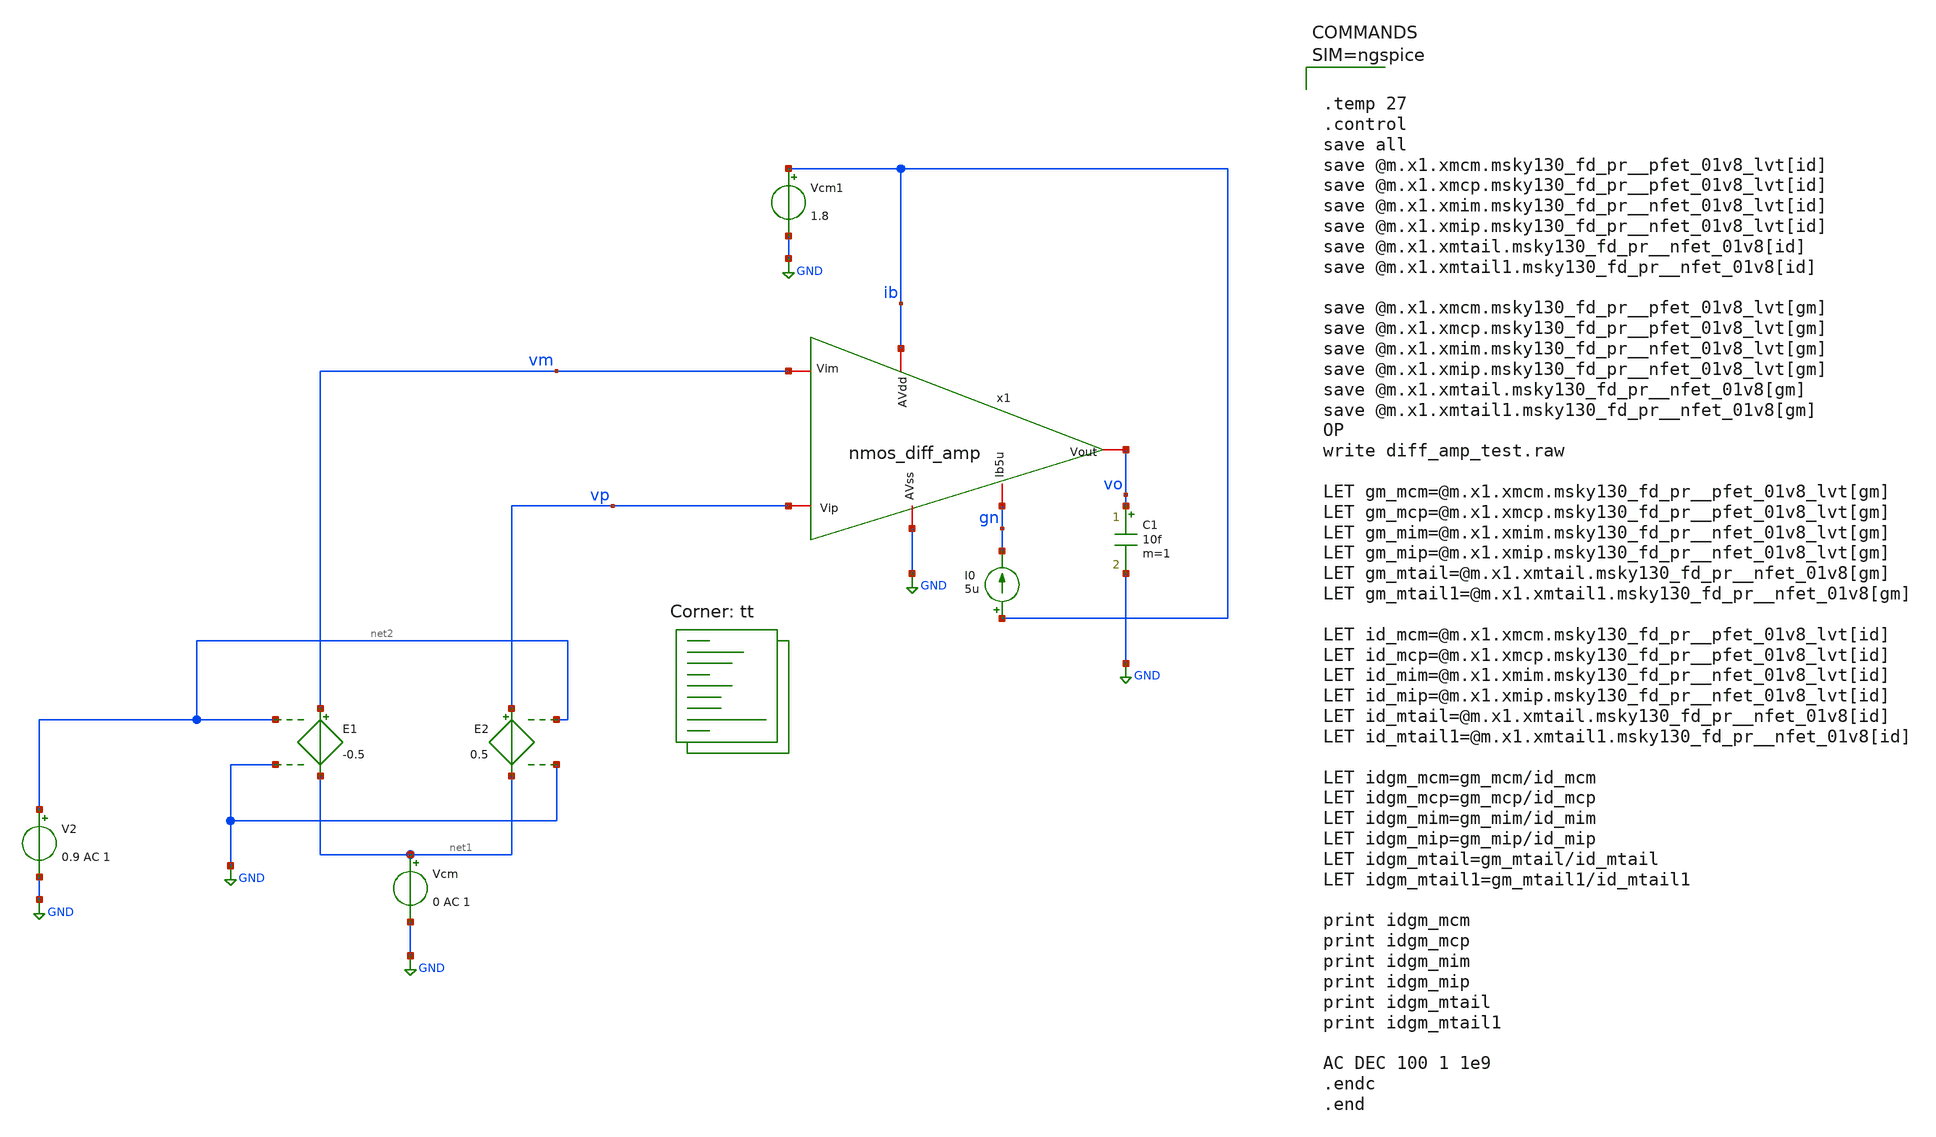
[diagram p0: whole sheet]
** sch_path: Work/xschem/diff_amp_test.sch
**.subckt diff_amp_test
x1 ib vo vm vp gn GND nmos_diff_amp
E1 vm net1 net2 GND -0.5
E2 vp net1 net2 GND 0.5
Vcm net1 GND 0 AC 1
V2 net2 GND 0.9 AC 1
Vcm1 ib GND 1.8
I0 ib gn 5u
C1 vo GND 10f m=1
**** begin user architecture code



.temp 27
.control
save all
save @m.x1.xmcm.msky130_fd_pr__pfet_01v8_lvt[id]
save @m.x1.xmcp.msky130_fd_pr__pfet_01v8_lvt[id]
save @m.x1.xmim.msky130_fd_pr__nfet_01v8_lvt[id]
save @m.x1.xmip.msky130_fd_pr__nfet_01v8_lvt[id]
save @m.x1.xmtail.msky130_fd_pr__nfet_01v8[id]
save @m.x1.xmtail1.msky130_fd_pr__nfet_01v8[id]

save @m.x1.xmcm.msky130_fd_pr__pfet_01v8_lvt[gm]
save @m.x1.xmcp.msky130_fd_pr__pfet_01v8_lvt[gm]
save @m.x1.xmim.msky130_fd_pr__nfet_01v8_lvt[gm]
save @m.x1.xmip.msky130_fd_pr__nfet_01v8_lvt[gm]
save @m.x1.xmtail.msky130_fd_pr__nfet_01v8[gm]
save @m.x1.xmtail1.msky130_fd_pr__nfet_01v8[gm]
OP
write diff_amp_test.raw

LET gm_mcm=@m.x1.xmcm.msky130_fd_pr__pfet_01v8_lvt[gm]
LET gm_mcp=@m.x1.xmcp.msky130_fd_pr__pfet_01v8_lvt[gm]
LET gm_mim=@m.x1.xmim.msky130_fd_pr__nfet_01v8_lvt[gm]
LET gm_mip=@m.x1.xmip.msky130_fd_pr__nfet_01v8_lvt[gm]
LET gm_mtail=@m.x1.xmtail.msky130_fd_pr__nfet_01v8[gm]
LET gm_mtail1=@m.x1.xmtail1.msky130_fd_pr__nfet_01v8[gm]

LET id_mcm=@m.x1.xmcm.msky130_fd_pr__pfet_01v8_lvt[id]
LET id_mcp=@m.x1.xmcp.msky130_fd_pr__pfet_01v8_lvt[id]
LET id_mim=@m.x1.xmim.msky130_fd_pr__nfet_01v8_lvt[id]
LET id_mip=@m.x1.xmip.msky130_fd_pr__nfet_01v8_lvt[id]
LET id_mtail=@m.x1.xmtail.msky130_fd_pr__nfet_01v8[id]
LET id_mtail1=@m.x1.xmtail1.msky130_fd_pr__nfet_01v8[id]

LET idgm_mcm=gm_mcm/id_mcm
LET idgm_mcp=gm_mcp/id_mcp
LET idgm_mim=gm_mim/id_mim
LET idgm_mip=gm_mip/id_mip
LET idgm_mtail=gm_mtail/id_mtail
LET idgm_mtail1=gm_mtail1/id_mtail1

print idgm_mcm
print idgm_mcp
print idgm_mim
print idgm_mip
print idgm_mtail
print idgm_mtail1

AC DEC 100 1 1e9
.endc
.end




.lib $::SKYWATER_MODELS/sky130.lib.spice tt
.lib /usr/local/share/pdk/sky130A/libs.tech/ngspice/sky130.lib.spice tt
**** end user architecture code
**.ends

* expanding   symbol:  nmos_diff_amp.sym # of pins=6
** sym_path: Work/xschem/nmos_diff_amp.sym
** sch_path: Work/xschem/nmos_diff_amp.sch
.subckt nmos_diff_amp AVdd Vout Vim Vip Ib5u AVss
*.iopin AVdd
*.iopin AVss
*.iopin Vim
*.iopin Vip
*.iopin Vout
*.iopin Ib5u
XMip vp Vip io io sky130_fd_pr__nfet_01v8_lvt L=2 W=5 nf=1 ad='int((1 + 1)/2) * 5 / 1 * 0.29' as='int((1 + 2)/2) * 5 / 1 * 0.29'
+ pd='2*int((1 + 1)/2) * (5 / 1 + 0.29)' ps='2*int((1 + 2)/2) * (5 / 1 + 0.29)' nrd='0.29 / 5 ' nrs='0.29 / 5 '
+ sa=0 sb=0 sd=0 mult=4 m=4
XMim Vout Vim io io sky130_fd_pr__nfet_01v8_lvt L=2 W=5 nf=1 ad='int((1 + 1)/2) * 5 / 1 * 0.29' as='int((1 + 2)/2) * 5 / 1 * 0.29'
+ pd='2*int((1 + 1)/2) * (5 / 1 + 0.29)' ps='2*int((1 + 2)/2) * (5 / 1 + 0.29)' nrd='0.29 / 5 ' nrs='0.29 / 5 '
+ sa=0 sb=0 sd=0 mult=4 m=4
XMcp vp vp AVdd AVdd sky130_fd_pr__pfet_01v8_lvt L=2 W=5 nf=1 ad='int((1 + 1)/2) * 5 / 1 * 0.29' as='int((1 + 2)/2) * 5 / 1 * 0.29'
+ pd='2*int((1 + 1)/2) * (5 / 1 + 0.29)' ps='2*int((1 + 2)/2) * (5 / 1 + 0.29)' nrd='0.29 / 5 ' nrs='0.29 / 5 '
+ sa=0 sb=0 sd=0 mult=2 m=2
XMcm Vout vp AVdd AVdd sky130_fd_pr__pfet_01v8_lvt L=2 W=5 nf=1 ad='int((1 + 1)/2) * 5 / 1 * 0.29' as='int((1 + 2)/2) * 5 / 1 * 0.29'
+ pd='2*int((1 + 1)/2) * (5 / 1 + 0.29)' ps='2*int((1 + 2)/2) * (5 / 1 + 0.29)' nrd='0.29 / 5 ' nrs='0.29 / 5 '
+ sa=0 sb=0 sd=0 mult=2 m=2
XMtail Ib5u Ib5u AVss AVss sky130_fd_pr__nfet_01v8 L=1 W=5 nf=1 ad='int((1 + 1)/2) * 5 / 1 * 0.29' as='int((1 + 2)/2) * 5 / 1 * 0.29'
+ pd='2*int((1 + 1)/2) * (5 / 1 + 0.29)' ps='2*int((1 + 2)/2) * (5 / 1 + 0.29)' nrd='0.29 / 5 ' nrs='0.29 / 5 '
+ sa=0 sb=0 sd=0 mult=1 m=1
XMtail1 io Ib5u AVss AVss sky130_fd_pr__nfet_01v8 L=1 W=5 nf=1 ad='int((1 + 1)/2) * 5 / 1 * 0.29' as='int((1 + 2)/2) * 5 / 1 * 0.29'
+ pd='2*int((1 + 1)/2) * (5 / 1 + 0.29)' ps='2*int((1 + 2)/2) * (5 / 1 + 0.29)' nrd='0.29 / 5 ' nrs='0.29 / 5 '
+ sa=0 sb=0 sd=0 mult=2 m=2
.ends

.GLOBAL GND
.end
